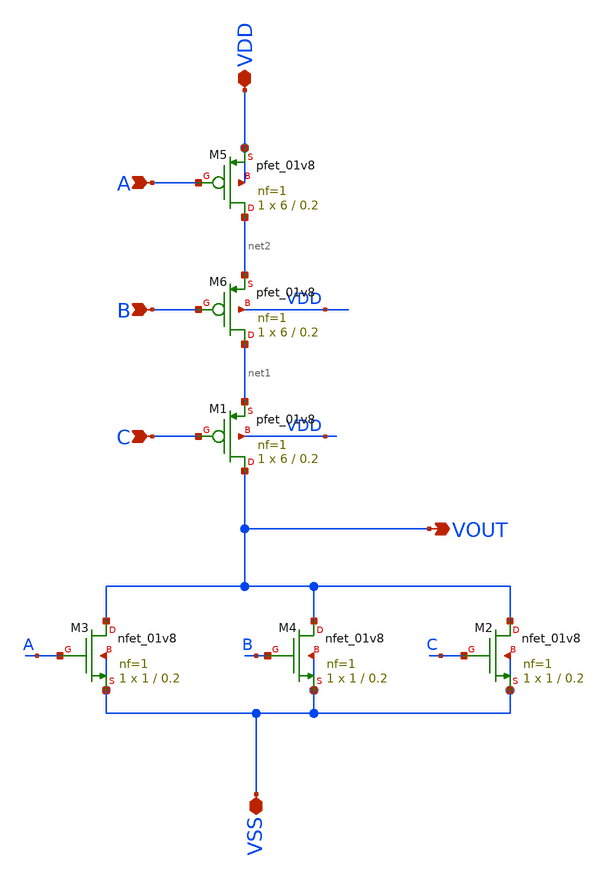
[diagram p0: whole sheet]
** sch_path: Xschem/PLL_TOP_Schematics/3_inp_NOR.sch
* Copyright 2022 GlobalFoundries PDK Authors
* Licensed under the Apache License, Version 2.0 (the "License");
* you may not use this file except in compliance with the License.
* You may obtain a copy of the License at
* https://www.apache.org/licenses/LICENSE-2.0
* Unless required by applicable law or agreed to in writing, software
* distributed under the License is distributed on an "AS IS" BASIS,
* WITHOUT WARRANTIES OR CONDITIONS OF ANY KIND, either express or implied.
* See the License for the specific language governing permissions and
* limitations under the License.
**.subckt 3_inp_NOR VSS VDD A B C VOUT
*.iopin VSS
*.iopin VDD
*.ipin A
*.ipin B
*.ipin C
*.opin VOUT
XM5 net2 A VDD VDD sky130_fd_pr__pfet_01v8 L=0.2 W=6 nf=1 ad='int((nf+1)/2) * W/nf * 0.29' as='int((nf+2)/2) * W/nf * 0.29'
+ pd='2*int((nf+1)/2) * (W/nf + 0.29)' ps='2*int((nf+2)/2) * (W/nf + 0.29)' nrd='0.29 / W' nrs='0.29 / W'
+ sa=0 sb=0 sd=0 mult=1 m=1
XM2 VOUT C VSS VSS sky130_fd_pr__nfet_01v8 L=0.2 W=1 nf=1 ad='int((nf+1)/2) * W/nf * 0.29' as='int((nf+2)/2) * W/nf * 0.29'
+ pd='2*int((nf+1)/2) * (W/nf + 0.29)' ps='2*int((nf+2)/2) * (W/nf + 0.29)' nrd='0.29 / W' nrs='0.29 / W'
+ sa=0 sb=0 sd=0 mult=1 m=1
XM3 VOUT A VSS VSS sky130_fd_pr__nfet_01v8 L=0.2 W=1 nf=1 ad='int((nf+1)/2) * W/nf * 0.29' as='int((nf+2)/2) * W/nf * 0.29'
+ pd='2*int((nf+1)/2) * (W/nf + 0.29)' ps='2*int((nf+2)/2) * (W/nf + 0.29)' nrd='0.29 / W' nrs='0.29 / W'
+ sa=0 sb=0 sd=0 mult=1 m=1
XM4 VOUT B VSS VSS sky130_fd_pr__nfet_01v8 L=0.2 W=1 nf=1 ad='int((nf+1)/2) * W/nf * 0.29' as='int((nf+2)/2) * W/nf * 0.29'
+ pd='2*int((nf+1)/2) * (W/nf + 0.29)' ps='2*int((nf+2)/2) * (W/nf + 0.29)' nrd='0.29 / W' nrs='0.29 / W'
+ sa=0 sb=0 sd=0 mult=1 m=1
XM1 VOUT C net1 VDD sky130_fd_pr__pfet_01v8 L=0.2 W=6 nf=1 ad='int((nf+1)/2) * W/nf * 0.29' as='int((nf+2)/2) * W/nf * 0.29'
+ pd='2*int((nf+1)/2) * (W/nf + 0.29)' ps='2*int((nf+2)/2) * (W/nf + 0.29)' nrd='0.29 / W' nrs='0.29 / W'
+ sa=0 sb=0 sd=0 mult=1 m=1
XM6 net1 B net2 VDD sky130_fd_pr__pfet_01v8 L=0.2 W=6 nf=1 ad='int((nf+1)/2) * W/nf * 0.29' as='int((nf+2)/2) * W/nf * 0.29'
+ pd='2*int((nf+1)/2) * (W/nf + 0.29)' ps='2*int((nf+2)/2) * (W/nf + 0.29)' nrd='0.29 / W' nrs='0.29 / W'
+ sa=0 sb=0 sd=0 mult=1 m=1
**.ends
.end
